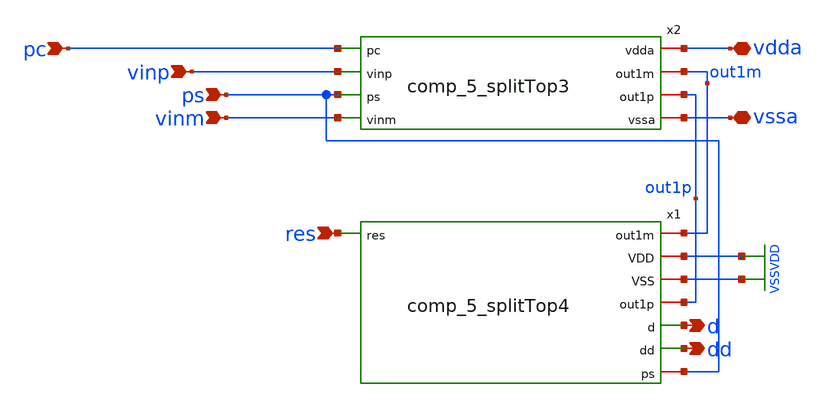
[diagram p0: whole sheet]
** sch_path: 5_Design/4_Layout/Team 5/xschem/comp_5_splitTop.sch
**.subckt comp_5_splitTop pc vdda vssa vinp ps vinm res dd d
*.ipin pc
*.iopin vdda
*.iopin vssa
*.ipin vinp
*.ipin ps
*.ipin vinm
*.ipin res
*.opin dd
*.opin d
x2 vdda pc out1m vinp out1p vssa ps vinm comp_5_splitTop3
x1 out1m VDD VSS out1p res d dd ps comp_5_splitTop4
**.ends
.GLOBAL VDD
.GLOBAL VSS
.end
